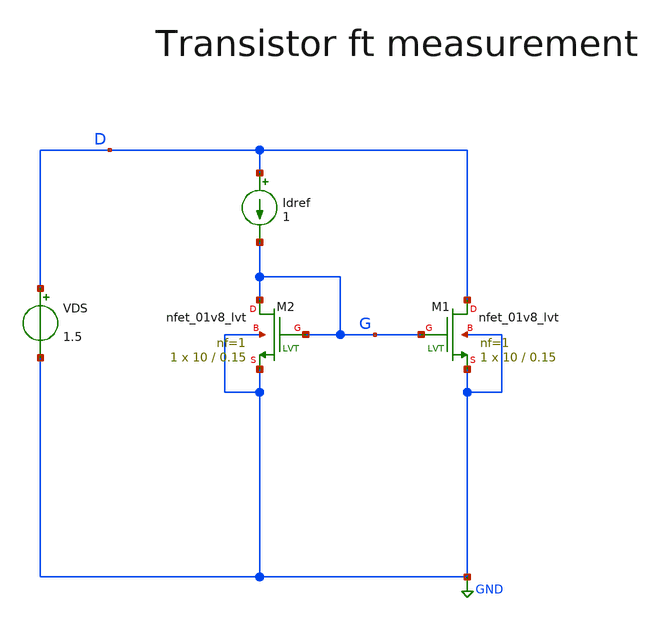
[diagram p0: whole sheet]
** sch_path: implementation/schematic/sky130_tests/tb_ft_test.sch
**.subckt tb_ft_test
XM1 D G GND GND sky130_fd_pr__nfet_01v8_lvt L=0.15 W=10 nf=1 ad='int((nf+1)/2) * W/nf * 0.29' as='int((nf+2)/2) * W/nf * 0.29'
+ pd='2*int((nf+1)/2) * (W/nf + 0.29)' ps='2*int((nf+2)/2) * (W/nf + 0.29)' nrd='0.29 / W' nrs='0.29 / W'
+ sa=0 sb=0 sd=0 mult=1 m=1
VDS D GND 1.5
Idref D G 1
XM2 G G GND GND sky130_fd_pr__nfet_01v8_lvt L=0.15 W=10 nf=1 ad='int((nf+1)/2) * W/nf * 0.29' as='int((nf+2)/2) * W/nf * 0.29'
+ pd='2*int((nf+1)/2) * (W/nf + 0.29)' ps='2*int((nf+2)/2) * (W/nf + 0.29)' nrd='0.29 / W' nrs='0.29 / W'
+ sa=0 sb=0 sd=0 mult=1 m=1
**** begin user architecture code



.options filetype=ascii
.save all

.op
.control
*dc Idref 0.1e-3 10e-3 0.1e-3

let n_idx = 101

let start_iref = 0.1e-3
let stop_iref = 10e-3
let delta_iref = (stop_iref - start_iref) / n_idx
let iref_act = start_iref

let vgs = unitvec(n_idx)
let gms = unitvec(n_idx)
let ids = unitvec(n_idx)

let cgss = unitvec(n_idx)
let cgds = unitvec(n_idx)

let idxs = 0
let idx = idxs

*loop
while iref_act le stop_iref
  alter idref iref_act
  run
  *print @m.xm2.msky130_fd_pr__nfet_01v8_lvt[gm]

  let gms[idx] = @m.xm2.msky130_fd_pr__nfet_01v8_lvt[gm]
  let ids[idx] = @m.xm2.msky130_fd_pr__nfet_01v8_lvt[id]

  let cgss[idx] = @m.xm2.msky130_fd_pr__nfet_01v8_lvt[cgs]
  let cgds[idx] = @m.xm2.msky130_fd_pr__nfet_01v8_lvt[cgd]
  let vgs[idx] = v(G)

  let iref_act = iref_act + delta_iref
  let idxs = idx + 1
  let idx = idxs
end

let ft = -gms/(2*pi*(cgss+cgds))
let gm_id = gms/ids
settype voltage vgs
settype current ids
setscale ids
plot xlog ft vs gm_id
plot gms vs ids
plot xlog ft vs ids
plot xlog vgs vs ids
write tb_ft_test.raw
.endc
.end



** opencircuitdesign pdks install
.lib /farmshare/home/classes/ee/372/PDKs/open_pdks/sky130/sky130A/libs.tech/ngspice/sky130.lib.spice tt


**** end user architecture code
**.ends
.GLOBAL GND
.end
